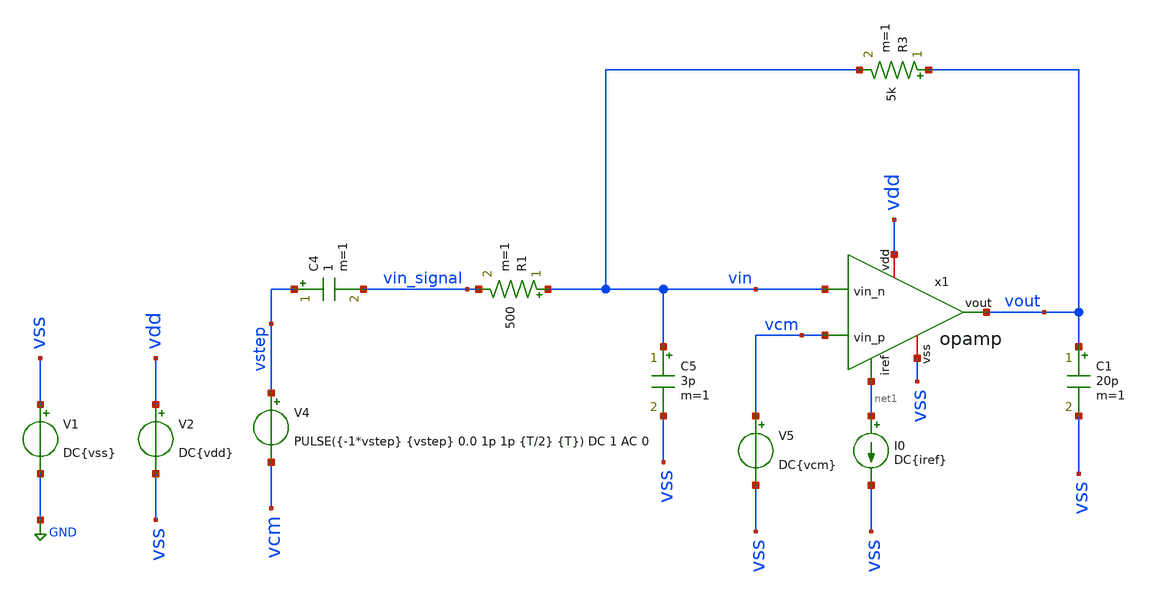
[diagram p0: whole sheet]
** sch_path: tb_opamp_stepresponse.sch
**.subckt tb_opamp_stepresponse
V1 vss GND DC{vss}
V2 vdd vss DC{vdd}
V4 vstep vcm PULSE({-1*vstep} {vstep} 0.0 1p 1p {T/2} {T}) DC 1 AC 0
C4 vstep vin_signal 1 m=1
I0 net1 vss DC{iref}
R1 vin vin_signal 500 m=1
R3 vout vin 5k m=1
C5 vin vss 3p m=1
C1 vout vss 20p m=1
V5 vcm vss DC{vcm}
x1 vdd net1 vin vcm vout vss opamp
**** begin user architecture code




* Circuit Parameters
.param iref = 100u
.param vdd  = 1.8
.param vss  = 0.0
.param vcm  = vdd/2
.param vac  = 10m
.param vstep = 60m
.param T = 20u

.options TEMP = 65

.param mul8 = 2
.param mul5 = 20
.param mul7 = 150
.param w857 = 70
.param l857 = 7

.param l34  = 3
.param w34  = 60
.param mul34 = 2

.param mpar = 333
.param lpar = 0.5
.param wpar = 10

.param mul6 = 90
.param l6   = 0.15
.param w6   = 25

.param mul9 = 1
.param l9   = 0.15
.param w9   = 10

.param res_1 = 333
.param cap_1 = 5p

* Include Models
.lib ~/skywater/skywater-pdk/libraries/sky130_fd_pr_ngspice/latest/models/corners/sky130.lib TT

* OP Parameters & Singals to save
.save all

*Simulations
.control
  set color0 = grey
  tran 0.01u 20u
  setplot tran1
  plot v(vstep) v(vin_signal) v(vout)

.endc

.end


**** end user architecture code
**.ends

* expanding   symbol:  opamp.sym # of pins=6
** sym_path: opamp.sym
** sch_path: opamp.sch
.subckt opamp vdd iref vin_n vin_p vout vss
*.iopin vdd
*.iopin vss
*.ipin vin_n
*.ipin vin_p
*.ipin iref
*.opin vout
XM3 vbn vbn vss vss sky130_fd_pr__nfet_01v8 L={L34} W={W34} nf=1 ad='W * 0.29' as='W * 0.29' pd='2 * (W + 0.29)'
+ ps='2 * (W + 0.29)' nrd='0.29 / W' nrs='0.29 / W' sa=0 sb=0 sd=0 mult={mul34} m={mul34}
XM4 voe1 vbn vss vss sky130_fd_pr__nfet_01v8 L={L34} W={W34} nf=1 ad='W * 0.29' as='W * 0.29' pd='2 * (W + 0.29)'
+ ps='2 * (W + 0.29)' nrd='0.29 / W' nrs='0.29 / W' sa=0 sb=0 sd=0 mult={mul34} m={mul34}
XM5 vp iref vdd vdd sky130_fd_pr__pfet_01v8 L={L857} W={W857} nf=1 ad='W * 0.29' as='W * 0.29' pd='2 * (W + 0.29)'
+ ps='2 * (W + 0.29)' nrd='0.29 / W' nrs='0.29 / W' sa=0 sb=0 sd=0 mult=20 m=20
XM7 vout iref vdd vdd sky130_fd_pr__pfet_01v8 L={L857} W={W857} nf=1 ad='W * 0.29' as='W * 0.29' pd='2 * (W + 0.29)'
+ ps='2 * (W + 0.29)' nrd='0.29 / W' nrs='0.29 / W' sa=0 sb=0 sd=0 mult=150 m=150
XM8 iref iref vdd vdd sky130_fd_pr__pfet_01v8 L={L857} W={W857} nf=1 ad='W * 0.29' as='W * 0.29' pd='2 * (W + 0.29)'
+ ps='2 * (W + 0.29)' nrd='0.29 / W' nrs='0.29 / W' sa=0 sb=0 sd=0 mult=2 m=2
XM9 vss vss vss vss sky130_fd_pr__nfet_01v8 L=0.15 W=1 nf=1 ad='W * 0.29' as='W * 0.29' pd='2 * (W + 0.29)'
+ ps='2 * (W + 0.29)' nrd='0.29 / W' nrs='0.29 / W' sa=0 sb=0 sd=0 mult=1 m=1
XM6 vout voe1 vss vss sky130_fd_pr__nfet_01v8 L=0.15 W=25 nf=1 ad='W * 0.29' as='W * 0.29' pd='2 * (W + 0.29)'
+ ps='2 * (W + 0.29)' nrd='0.29 / W' nrs='0.29 / W' sa=0 sb=0 sd=0 mult=90 m=90
XM1 vbn vin_n vp vp sky130_fd_pr__pfet_01v8_lvt L={lpar} W={wpar} nf=1 ad='int((nf+1)/2) * W/nf * 0.29'
+ as='int((nf+2)/2) * W/nf * 0.29' pd='2*int((nf+1)/2) * (W/nf + 0.29)' ps='2*int((nf+2)/2) * (W/nf + 0.29)'
+ nrd='0.29 / W' nrs='0.29 / W' sa=0 sb=0 sd=0 mult={mpar} m={mpar}
XM2 voe1 vin_p vp vp sky130_fd_pr__pfet_01v8_lvt L={lpar} W={wpar} nf=1 ad='int((nf+1)/2) * W/nf * 0.29'
+ as='int((nf+2)/2) * W/nf * 0.29' pd='2*int((nf+1)/2) * (W/nf + 0.29)' ps='2*int((nf+2)/2) * (W/nf + 0.29)'
+ nrd='0.29 / W' nrs='0.29 / W' sa=0 sb=0 sd=0 mult={mpar} m={mpar}
C1 net1 vout 3.1p m=1
R1 net1 voe1 333 m=1
.ends

.GLOBAL GND
.end
